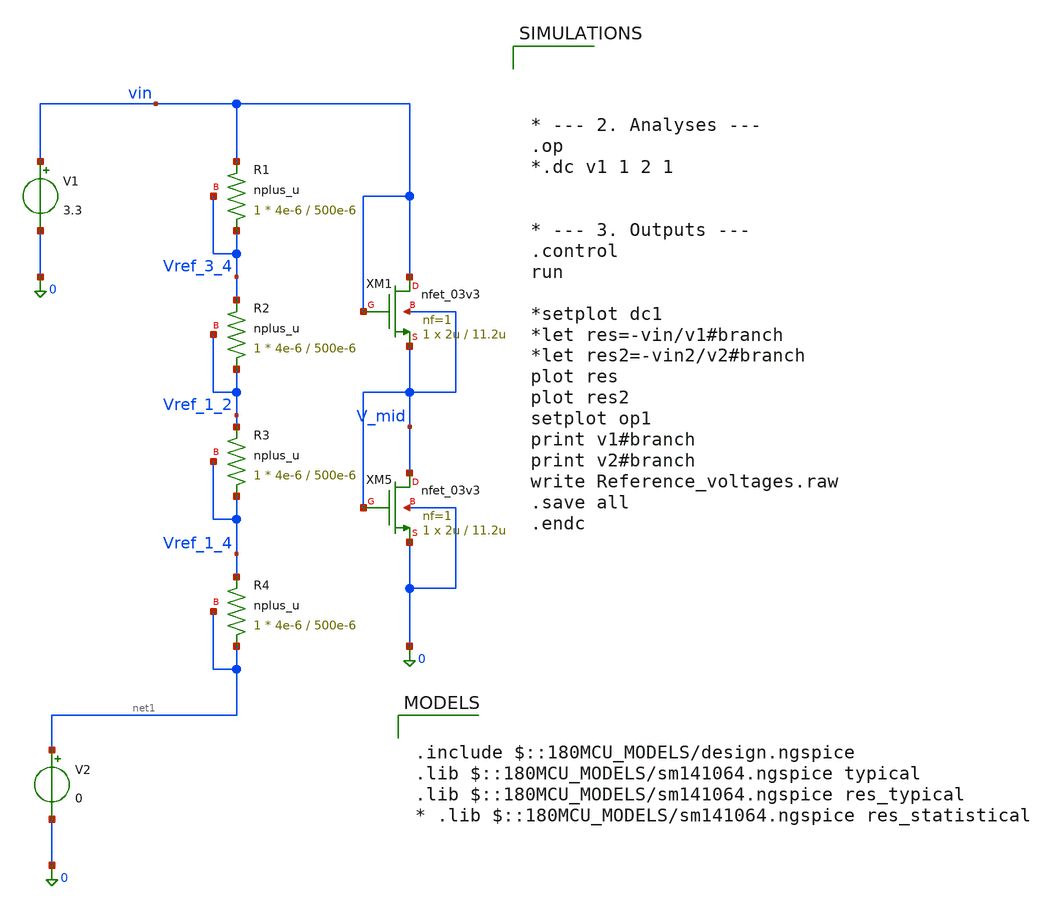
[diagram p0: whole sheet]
** sch_path: Felix/Reference_voltages.sch
**.subckt Reference_voltages
XR1 Vref_3_4 vin Vref_3_4 nplus_u r_width=4e-6 r_length=500e-6 m=1
V1 vin 0 3.3
XR2 Vref_1_2 Vref_3_4 Vref_1_2 nplus_u r_width=4e-6 r_length=500e-6 m=1
XR3 Vref_1_4 Vref_1_2 Vref_1_4 nplus_u r_width=4e-6 r_length=500e-6 m=1
V2 net1 0 0
XR4 net1 Vref_1_4 net1 nplus_u r_width=4e-6 r_length=500e-6 m=1
XM5 V_mid V_mid 0 0 nfet_03v3 L=11.2u W=2u nf=1 ad='int((nf+1)/2) * W/nf * 0.18u' as='int((nf+2)/2) * W/nf * 0.18u'
+ pd='2*int((nf+1)/2) * (W/nf + 0.18u)' ps='2*int((nf+2)/2) * (W/nf + 0.18u)' nrd='0.18u / W' nrs='0.18u / W'
+ sa=0 sb=0 sd=0 m=1
XM1 vin vin V_mid V_mid nfet_03v3 L=11.2u W=2u nf=1 ad='int((nf+1)/2) * W/nf * 0.18u' as='int((nf+2)/2) * W/nf * 0.18u'
+ pd='2*int((nf+1)/2) * (W/nf + 0.18u)' ps='2*int((nf+2)/2) * (W/nf + 0.18u)' nrd='0.18u / W' nrs='0.18u / W'
+ sa=0 sb=0 sd=0 m=1
**** begin user architecture code




* --- 2. Analyses ---
.op
*.dc v1 1 2 1


* --- 3. Outputs ---
.control
run

*setplot dc1
*let res=-vin/v1#branch
*let res2=-vin2/v2#branch
plot res
plot res2
setplot op1
print v1#branch
print v2#branch
write Reference_voltages.raw
.save all
.endc





.include $::180MCU_MODELS/design.ngspice
.lib $::180MCU_MODELS/sm141064.ngspice typical
.lib $::180MCU_MODELS/sm141064.ngspice res_typical
* .lib $::180MCU_MODELS/sm141064.ngspice res_statistical

**** end user architecture code
**.ends
.end
